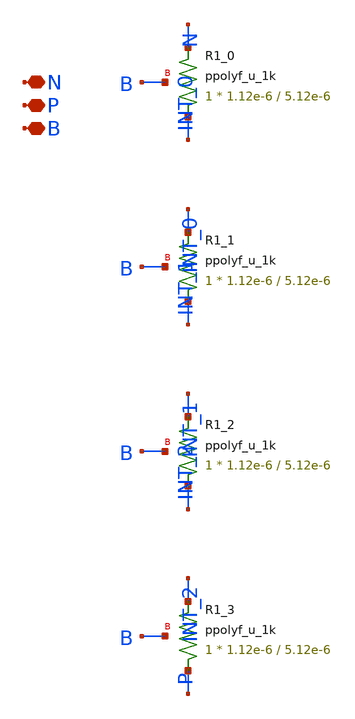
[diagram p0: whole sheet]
** sch_path: design/LELO_TR_GF180MCUD/LELOTR_RES4.sch
**.subckt LELOTR_RES4 N P B
*.iopin N
*.iopin P
*.iopin B
XR1_0 INT_0 N B ppolyf_u_1k r_width=1.12e-6 r_length=5.12e-6 m=1
XR1_1 INT_1 INT_0 B ppolyf_u_1k r_width=1.12e-6 r_length=5.12e-6 m=1
XR1_2 INT_2 INT_1 B ppolyf_u_1k r_width=1.12e-6 r_length=5.12e-6 m=1
XR1_3 P INT_2 B ppolyf_u_1k r_width=1.12e-6 r_length=5.12e-6 m=1
**.ends
.end
